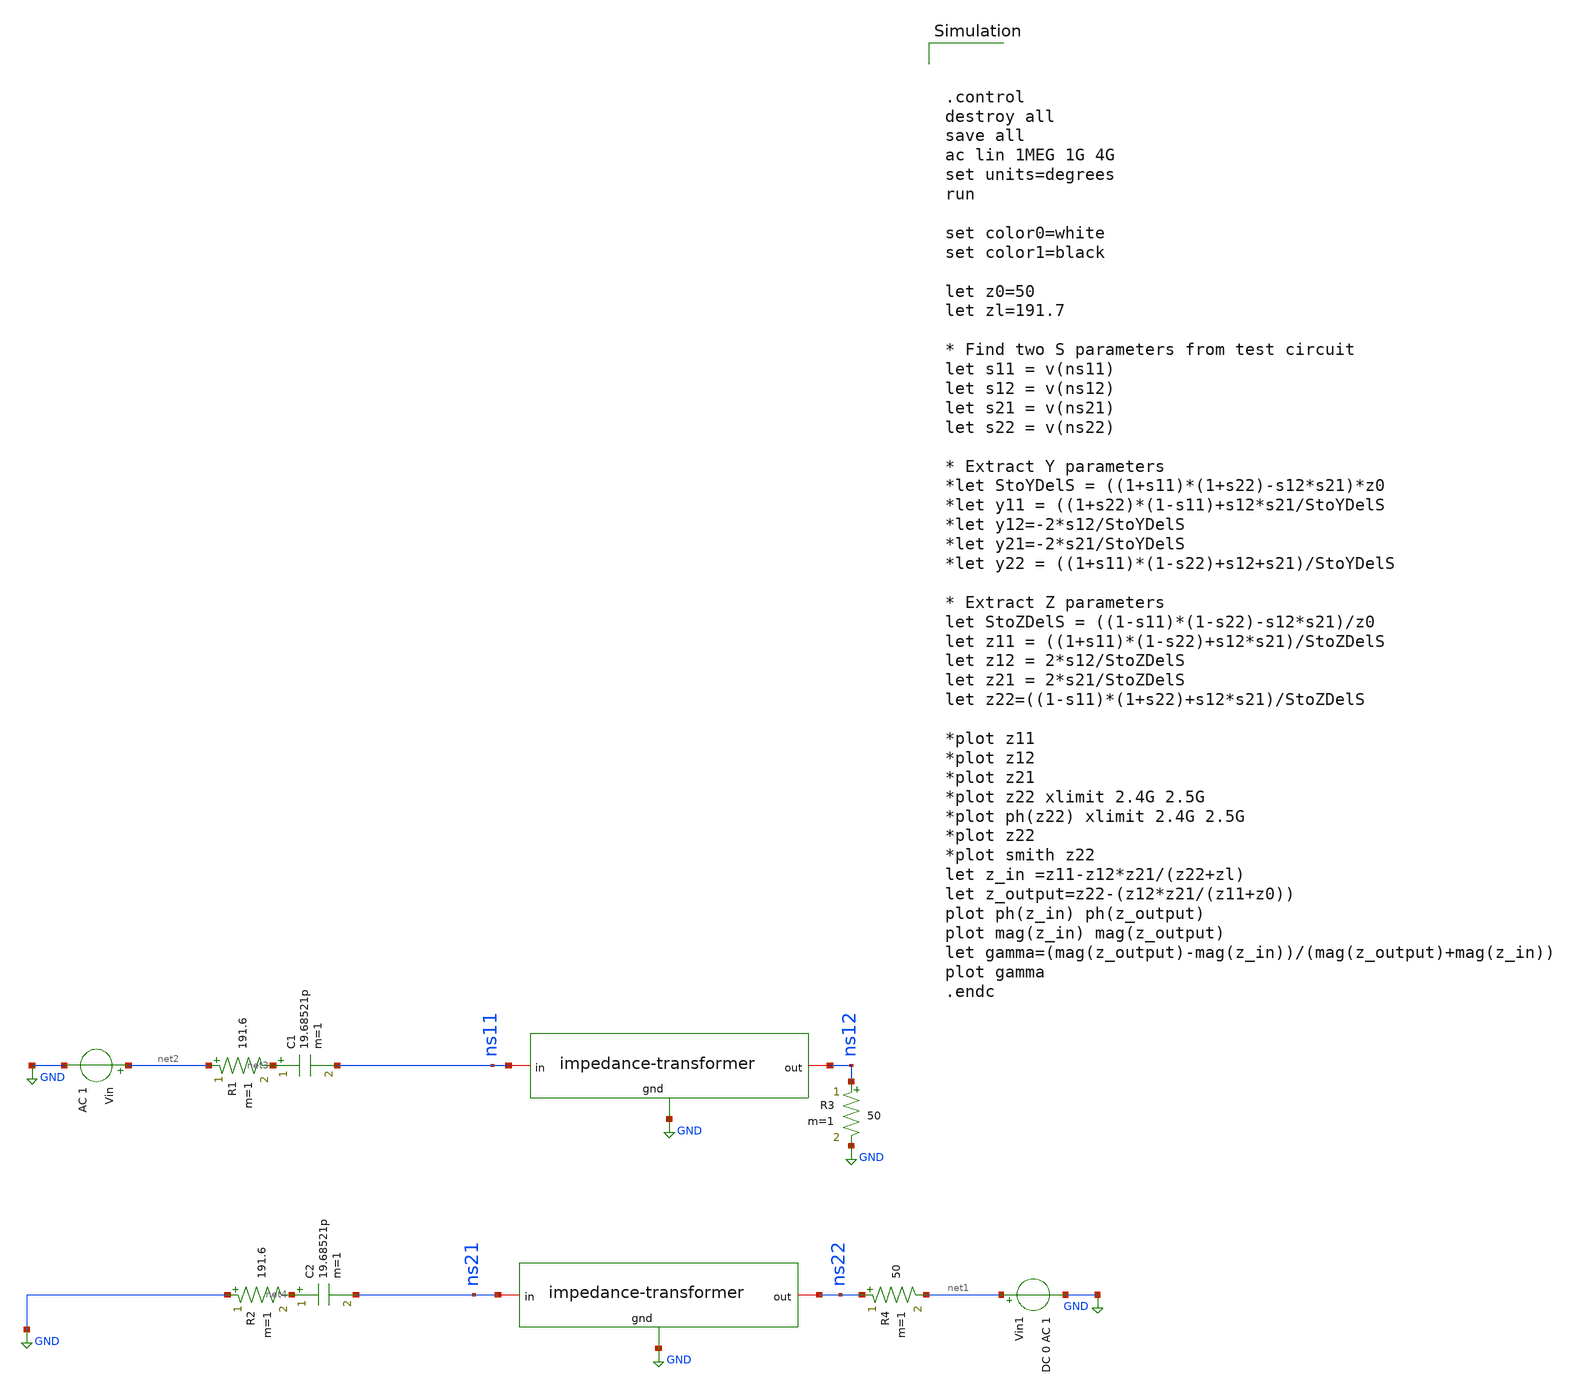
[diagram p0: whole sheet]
** sch_path: impedance-transformer/xschem/impedance-transformer_tb-ac.sch
**.subckt impedance-transformer_tb-ac
Vin1 net1 GND DC 0 AC 1
R3 ns12 GND 50 m=1
R4 ns22 net1 50 m=1
Vin net2 GND AC 1
R1 net2 net3 191.6 m=1
C1 net3 ns11 19.68521p m=1
R2 GND net4 191.6 m=1
C2 net4 ns21 19.68521p m=1
x1 ns11 ns12 GND impedance-transformer
x2 ns21 ns22 GND impedance-transformer
**** begin user architecture code



.control
destroy all
save all
ac lin 1MEG 1G 4G
set units=degrees
run

set color0=white
set color1=black

let z0=50
let zl=191.7

* Find two S parameters from test circuit
let s11 = v(ns11)
let s12 = v(ns12)
let s21 = v(ns21)
let s22 = v(ns22)

* Extract Y parameters
*let StoYDelS = ((1+s11)*(1+s22)-s12*s21)*z0
*let y11 = ((1+s22)*(1-s11)+s12*s21/StoYDelS
*let y12=-2*s12/StoYDelS
*let y21=-2*s21/StoYDelS
*let y22 = ((1+s11)*(1-s22)+s12+s21)/StoYDelS

* Extract Z parameters
let StoZDelS = ((1-s11)*(1-s22)-s12*s21)/z0
let z11 = ((1+s11)*(1-s22)+s12*s21)/StoZDelS
let z12 = 2*s12/StoZDelS
let z21 = 2*s21/StoZDelS
let z22=((1-s11)*(1+s22)+s12*s21)/StoZDelS

*plot z11
*plot z12
*plot z21
*plot z22 xlimit 2.4G 2.5G
*plot ph(z22) xlimit 2.4G 2.5G
*plot z22
*plot smith z22
let z_in =z11-z12*z21/(z22+zl)
let z_output=z22-(z12*z21/(z11+z0))
plot ph(z_in) ph(z_output)
plot mag(z_in) mag(z_output)
let gamma=(mag(z_output)-mag(z_in))/(mag(z_output)+mag(z_in))
plot gamma
.endc

 .lib $::SKYWATER_MODELS/sky130.lib.spice tt
.include $::SKYWATER_STDCELLS/sky130_fd_sc_hd.spice

**** end user architecture code
**.ends

* expanding   symbol:
*+  /home/hugodg/projects-sky130/temp-sensor/impedance-transformer/xschem/impedance-transformer.sym # of pins=3
** sym_path: impedance-transformer/xschem/impedance-transformer.sym
** sch_path: impedance-transformer/xschem/impedance-transformer.sch
.subckt impedance-transformer in out gnd
*.iopin gnd
*.iopin in
*.iopin out
XC0 in gnd sky130_fd_pr__cap_mim_m3_2 W=22.93 L=22.93 MF=9 m=9
XC1 out gnd sky130_fd_pr__cap_mim_m3_2 W=24.07 L=24.07 MF=16 m=16
x1 in out l1
**** begin user architecture code

* NGSPICE file created from impedance-transformer.ext - technology: sky130A

R0 in in.n1 0.704
R1 in.n0 in.t3 0.125
R2 in.n1 in.n0 0.089
R3 in.t8 in.t7 0.066
R4 in.t6 in.t8 0.066
R5 in.t2 in.t1 0.066
R6 in.t0 in.t2 0.066
R7 in.t5 in.t4 0.066
R8 in.t3 in.t5 0.066
R9 in.n1 in.t6 0.037
R10 in.n0 in.t0 0.037
R11 out out.n2 0.325
R12 out.n0 out.t13 0.094
R13 out.n1 out.n0 0.079
R14 out.t14 out.t15 0.066
R15 out.t12 out.t14 0.066
R16 out.t13 out.t12 0.066
R17 out.t10 out.t11 0.066
R18 out.t8 out.t10 0.066
R19 out.t9 out.t8 0.066
R20 out.t6 out.t7 0.066
R21 out.t4 out.t6 0.066
R22 out.t5 out.t4 0.066
R23 out.t2 out.t3 0.066
R24 out.t0 out.t2 0.066
R25 out.t1 out.t0 0.066
R26 out.n2 out.n1 0.064
R27 out.n2 out.t1 0.041
R28 out.n0 out.t9 0.018
R29 out.n1 out.t5 0.018
C0 out.t7 gnd 33.56fF
C1 out.t6 gnd 33.64fF
C2 out.t4 gnd 33.64fF
C3 out.t5 gnd 29.89fF
C4 out.t11 gnd 33.56fF
C5 out.t10 gnd 33.64fF
C6 out.t8 gnd 33.64fF
C7 out.t9 gnd 29.89fF
C8 out.t15 gnd 33.56fF
C9 out.t14 gnd 33.64fF
C10 out.t12 gnd 33.64fF
C11 out.t13 gnd 89.97fF
C12 out.n0 gnd 28.18fF $ **FLOATING
C13 out.n1 gnd 13.26fF $ **FLOATING
C14 out.t3 gnd 33.56fF
C15 out.t2 gnd 33.64fF
C16 out.t0 gnd 33.64fF
C17 out.t1 gnd 33.03fF
C18 out.n2 gnd 41.48fF $ **FLOATING
C19 in.t7 gnd 32.16fF
C20 in.t8 gnd 32.25fF
C21 in.t6 gnd 30.87fF
C22 in.t1 gnd 32.16fF
C23 in.t2 gnd 32.25fF
C24 in.t0 gnd 30.87fF
C25 in.t4 gnd 32.16fF
C26 in.t5 gnd 32.25fF
C27 in.t3 gnd 30.02fF
C28 in.n0 gnd 11.26fF $ **FLOATING
C29 in.n1 gnd 57.09fF $ **FLOATING
C30 in gnd 55.98fF
C31 out gnd 70.58fF




**** end user architecture code
.ends


* expanding   symbol:  /home/hugodg/projects-sky130/temp-sensor/impedance-transformer/xschem/l1.sym
*+ # of pins=2
** sym_path: impedance-transformer/xschem/l1.sym
** sch_path: impedance-transformer/xschem/l1.sch
.subckt l1 p1 p2
*.iopin p2
*.iopin p1
L0 p1 net3 598p m=1
Cs1 p1 net1 26.59f m=1
Cs2 p2 net2 25.14f m=1
Rs1 net1 GND 63.55 m=1
Rs2 net2 GND 19.11 m=1
R1 p2 net3 2.89 m=1
.ends

.GLOBAL GND
.end
